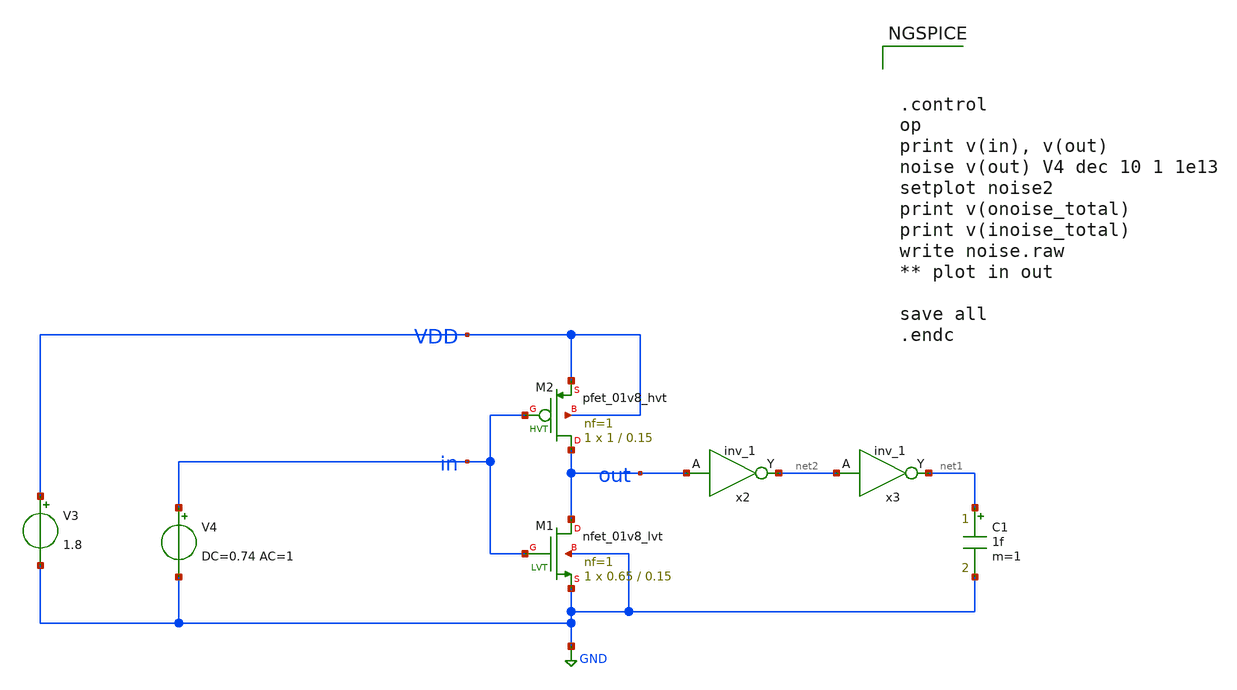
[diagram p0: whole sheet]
** sch_path: design/inverter_noise.sch
**.subckt inverter_noise
C1 net1 GND 1f m=1
XM1 out in GND GND sky130_fd_pr__nfet_01v8_lvt L=0.15 W=0.65 nf=1 ad='int((nf+1)/2) * W/nf * 0.29' as='int((nf+2)/2) * W/nf * 0.29'
+ pd='2*int((nf+1)/2) * (W/nf + 0.29)' ps='2*int((nf+2)/2) * (W/nf + 0.29)' nrd='0.29 / W' nrs='0.29 / W'
+ sa=0 sb=0 sd=0 mult=1 m=1
XM2 out in VDD VDD sky130_fd_pr__pfet_01v8_hvt L=0.15 W=1 nf=1 ad='int((nf+1)/2) * W/nf * 0.29' as='int((nf+2)/2) * W/nf * 0.29'
+ pd='2*int((nf+1)/2) * (W/nf + 0.29)' ps='2*int((nf+2)/2) * (W/nf + 0.29)' nrd='0.29 / W' nrs='0.29 / W'
+ sa=0 sb=0 sd=0 mult=1 m=1
V3 VDD GND 1.8
V4 in GND DC=0.74 AC=1
x2 out 0 0 VDD VDD net2 sky130_fd_sc_hd__inv_1
x3 net2 0 0 VDD VDD net1 sky130_fd_sc_hd__inv_1
**** begin user architecture code

** opencircuitdesign pdks install
.lib $::SKYWATER_MODELS/sky130.lib.spice tt_mm
.include $::SKYWATER_STDCELLS/sky130_fd_sc_hd.spice





.control
op
print v(in), v(out)
noise v(out) V4 dec 10 1 1e13
setplot noise2
print v(onoise_total)
print v(inoise_total)
write noise.raw
** plot in out

save all
.endc


**** end user architecture code
**.ends
.GLOBAL GND
.end
